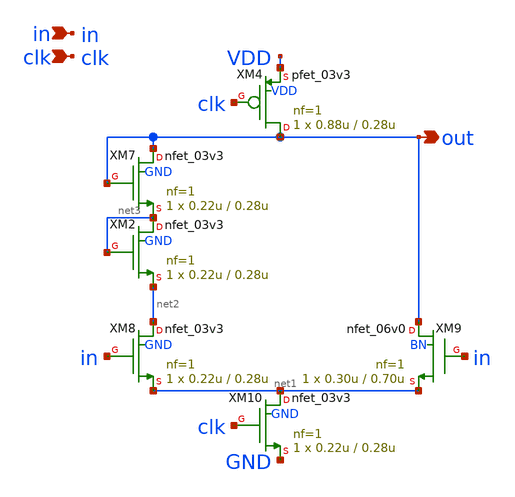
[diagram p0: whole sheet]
** sch_path: xschem_designs/STI_dyn.sch
**.subckt STI_dyn in out clk
*.ipin in
*.opin out
*.ipin clk
XM4 out clk VDD VDD pfet_03v3 L=0.28u W=0.88u nf=1 ad='int((nf+1)/2) * W/nf * 0.18u' as='int((nf+2)/2) * W/nf * 0.18u'
+ pd='2*int((nf+1)/2) * (W/nf + 0.18u)' ps='2*int((nf+2)/2) * (W/nf + 0.18u)' nrd='0.18u / W' nrs='0.18u / W'
+ sa=0 sb=0 sd=0 m=1 par=1
XM7 out out net3 GND nfet_03v3 L=0.28u W=0.22u nf=1 ad='int((nf+1)/2) * W/nf * 0.18u' as='int((nf+2)/2) * W/nf * 0.18u'
+ pd='2*int((nf+1)/2) * (W/nf + 0.18u)' ps='2*int((nf+2)/2) * (W/nf + 0.18u)' nrd='0.18u / W' nrs='0.18u / W'
+ sa=0 sb=0 sd=0 m=1 par=1
XM2 net3 net3 net2 GND nfet_03v3 L=0.28u W=0.22u nf=1 ad='int((nf+1)/2) * W/nf * 0.18u' as='int((nf+2)/2) * W/nf * 0.18u'
+ pd='2*int((nf+1)/2) * (W/nf + 0.18u)' ps='2*int((nf+2)/2) * (W/nf + 0.18u)' nrd='0.18u / W' nrs='0.18u / W'
+ sa=0 sb=0 sd=0 m=1 par=1
XM8 net2 in net1 GND nfet_03v3 L=0.28u W=0.22u nf=1 ad='int((nf+1)/2) * W/nf * 0.18u' as='int((nf+2)/2) * W/nf * 0.18u'
+ pd='2*int((nf+1)/2) * (W/nf + 0.18u)' ps='2*int((nf+2)/2) * (W/nf + 0.18u)' nrd='0.18u / W' nrs='0.18u / W'
+ sa=0 sb=0 sd=0 m=1 par=1
XM9 out in net1 BN nfet_06v0 L=0.70u W=0.30u nf=1 ad='int((nf+1)/2) * W/nf * 0.18u' as='int((nf+2)/2) * W/nf * 0.18u'
+ pd='2*int((nf+1)/2) * (W/nf + 0.18u)' ps='2*int((nf+2)/2) * (W/nf + 0.18u)' nrd='0.18u / W' nrs='0.18u / W'
+ sa=0 sb=0 sd=0 m=1 par=1
XM10 net1 clk GND GND nfet_03v3 L=0.28u W=0.22u nf=1 ad='int((nf+1)/2) * W/nf * 0.18u' as='int((nf+2)/2) * W/nf * 0.18u'
+ pd='2*int((nf+1)/2) * (W/nf + 0.18u)' ps='2*int((nf+2)/2) * (W/nf + 0.18u)' nrd='0.18u / W' nrs='0.18u / W'
+ sa=0 sb=0 sd=0 m=1 par=1
**.ends
.end
